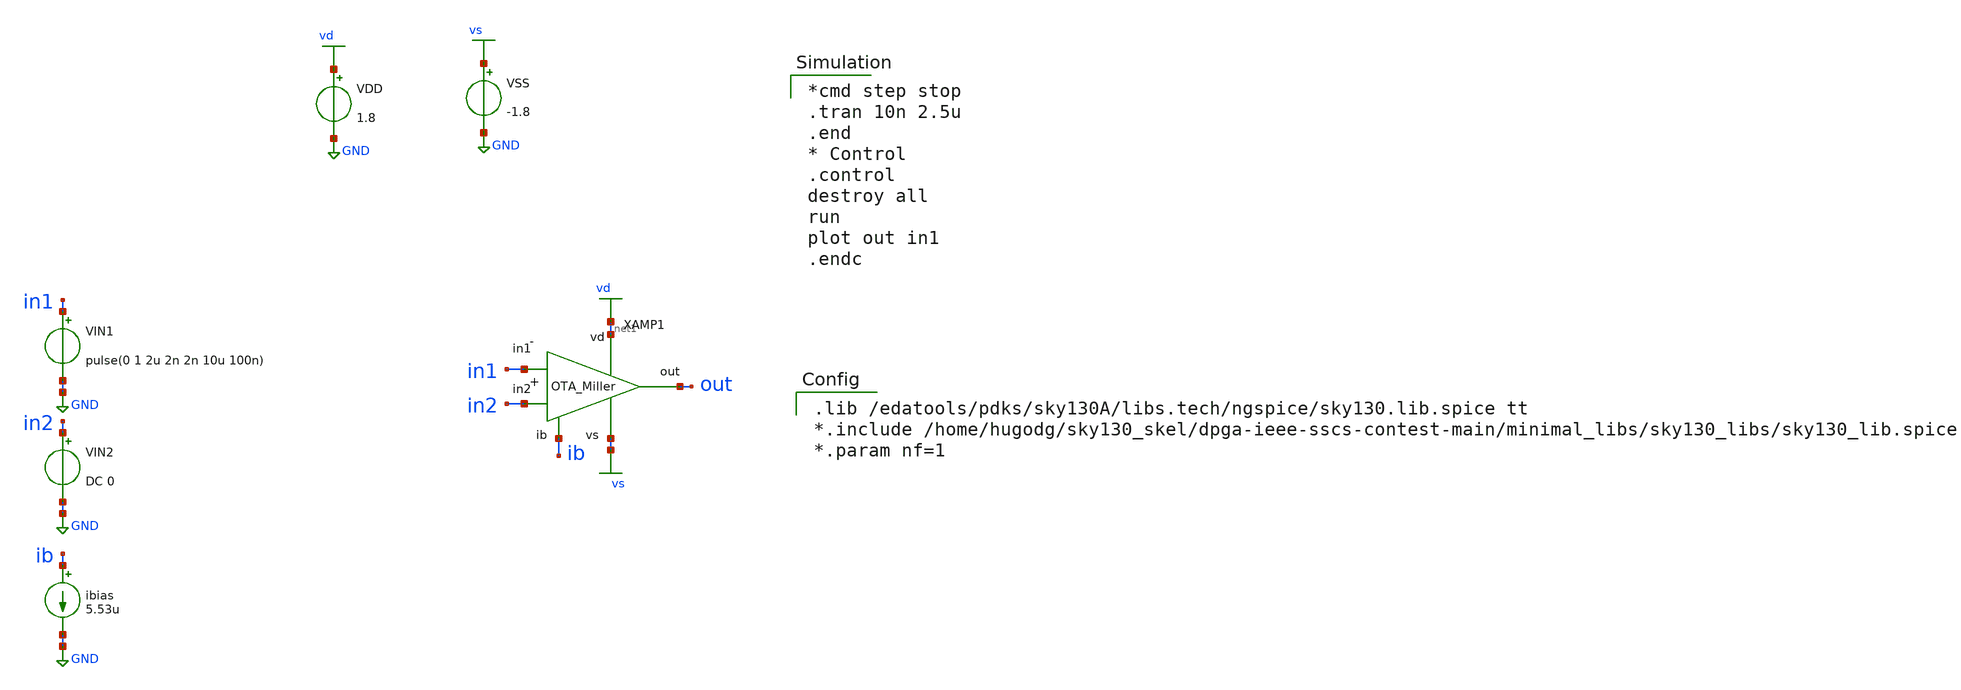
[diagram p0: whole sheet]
** sch_path: xschem/ota_tb-largesignal.sch
* Copyright 2020 Stefan Frederik Schippers
* Licensed under the Apache License, Version 2.0 (the "License");
* you may not use this file except in compliance with the License.
* You may obtain a copy of the License at
* https://www.apache.org/licenses/LICENSE-2.0
* Unless required by applicable law or agreed to in writing, software
* distributed under the License is distributed on an "AS IS" BASIS,
* WITHOUT WARRANTIES OR CONDITIONS OF ANY KIND, either express or implied.
* See the License for the specific language governing permissions and
* limitations under the License.
**.subckt ota_tb-largesignal
VIN2 in2 GND DC 0
VIN1 in1 GND pulse(0 1 2u 2n 2n 10u 100n)
ibias ib GND 5.53u
VDD vd GND 1.8
VSS vs GND -1.8
X1 net1 ib out in2 in1 vs ota
**** begin user architecture code

*cmd step stop
.tran 10n 2.5u
.end
* Control
.control
destroy all
run
plot out in1
.endc


.lib /edatools/pdks/sky130A/libs.tech/ngspice/sky130.lib.spice tt
*.include /home/hugodg/sky130_skel/dpga-ieee-sscs-contest-main/minimal_libs/sky130_libs/sky130_lib.spice
*.param nf=1

**** end user architecture code
**.ends

* expanding   symbol:  /home/hugodg/sky130_skel/dpga-ieee-sscs-contest-main/xschem/ota.sym # of
*+ pins=6
** sym_path: xschem/ota.sym
** sch_path: xschem/ota.sch
.subckt ota vd ib out in2 in1 vs
*.iopin vd
*.opin out
*.iopin vs
*.iopin ib
*.ipin in1
*.ipin in2
Cc net1 net4 0.5p m=1
XM4 net4 net3 vs vs sky130_fd_pr__nfet_01v8 L=1 W=0.861 nf=1 ad='int((nf+1)/2) * W/nf * 0.29' as='int((nf+2)/2) * W/nf * 0.29'
+ pd='2*int((nf+1)/2) * (W/nf + 0.29)' ps='2*int((nf+2)/2) * (W/nf + 0.29)' nrd='0.29 / W' nrs='0.29 / W'
+ sa=0 sb=0 sd=0 mult=1 m=1
XM7 net1 net4 vs vs sky130_fd_pr__nfet_01v8 L=1 W=8.61 nf=1 ad='int((nf+1)/2) * W/nf * 0.29' as='int((nf+2)/2) * W/nf * 0.29'
+ pd='2*int((nf+1)/2) * (W/nf + 0.29)' ps='2*int((nf+2)/2) * (W/nf + 0.29)' nrd='0.29 / W' nrs='0.29 / W'
+ sa=0 sb=0 sd=0 mult=1 m=1
XM5 ib ib vd vd sky130_fd_pr__pfet_01v8 L=1 W=5.85 nf=1 ad='int((nf+1)/2) * W/nf * 0.29' as='int((nf+2)/2) * W/nf * 0.29'
+ pd='2*int((nf+1)/2) * (W/nf + 0.29)' ps='2*int((nf+2)/2) * (W/nf + 0.29)' nrd='0.29 / W' nrs='0.29 / W'
+ sa=0 sb=0 sd=0 mult=1 m=1
XM6 net2 ib vd vd sky130_fd_pr__pfet_01v8 L=1 W=5.85 nf=1 ad='int((nf+1)/2) * W/nf * 0.29' as='int((nf+2)/2) * W/nf * 0.29'
+ pd='2*int((nf+1)/2) * (W/nf + 0.29)' ps='2*int((nf+2)/2) * (W/nf + 0.29)' nrd='0.29 / W' nrs='0.29 / W'
+ sa=0 sb=0 sd=0 mult=1 m=1
XM8 net1 ib vd vd sky130_fd_pr__pfet_01v8 L=1 W=29.3 nf=1 ad='int((nf+1)/2) * W/nf * 0.29' as='int((nf+2)/2) * W/nf * 0.29'
+ pd='2*int((nf+1)/2) * (W/nf + 0.29)' ps='2*int((nf+2)/2) * (W/nf + 0.29)' nrd='0.29 / W' nrs='0.29 / W'
+ sa=0 sb=0 sd=0 mult=1 m=1
XM10 out ib vd vd sky130_fd_pr__pfet_01v8 L=1 W=5.85 nf=1 ad='int((nf+1)/2) * W/nf * 0.29' as='int((nf+2)/2) * W/nf * 0.29'
+ pd='2*int((nf+1)/2) * (W/nf + 0.29)' ps='2*int((nf+2)/2) * (W/nf + 0.29)' nrd='0.29 / W' nrs='0.29 / W'
+ sa=0 sb=0 sd=0 mult=1 m=1
XM9 vs net1 out out sky130_fd_pr__pfet_01v8 L=1 W=5.85 nf=1 ad='int((nf+1)/2) * W/nf * 0.29' as='int((nf+2)/2) * W/nf * 0.29'
+ pd='2*int((nf+1)/2) * (W/nf + 0.29)' ps='2*int((nf+2)/2) * (W/nf + 0.29)' nrd='0.29 / W' nrs='0.29 / W'
+ sa=0 sb=0 sd=0 mult=1 m=1
XM1 net3 in1 net2 net2 sky130_fd_pr__pfet_01v8 L=1 W=2.93 nf=1 ad='int((nf+1)/2) * W/nf * 0.29' as='int((nf+2)/2) * W/nf * 0.29'
+ pd='2*int((nf+1)/2) * (W/nf + 0.29)' ps='2*int((nf+2)/2) * (W/nf + 0.29)' nrd='0.29 / W' nrs='0.29 / W'
+ sa=0 sb=0 sd=0 mult=1 m=1
XM2 net4 in2 net2 net2 sky130_fd_pr__pfet_01v8 L=1 W=2.93 nf=1 ad='int((nf+1)/2) * W/nf * 0.29' as='int((nf+2)/2) * W/nf * 0.29'
+ pd='2*int((nf+1)/2) * (W/nf + 0.29)' ps='2*int((nf+2)/2) * (W/nf + 0.29)' nrd='0.29 / W' nrs='0.29 / W'
+ sa=0 sb=0 sd=0 mult=1 m=1
XM3 net3 net3 vs vs sky130_fd_pr__nfet_01v8 L=1 W=0.861 nf=1 ad='int((nf+1)/2) * W/nf * 0.29' as='int((nf+2)/2) * W/nf * 0.29'
+ pd='2*int((nf+1)/2) * (W/nf + 0.29)' ps='2*int((nf+2)/2) * (W/nf + 0.29)' nrd='0.29 / W' nrs='0.29 / W'
+ sa=0 sb=0 sd=0 mult=1 m=1
.ends

.GLOBAL GND
.GLOBAL vd
.GLOBAL vs
.end
